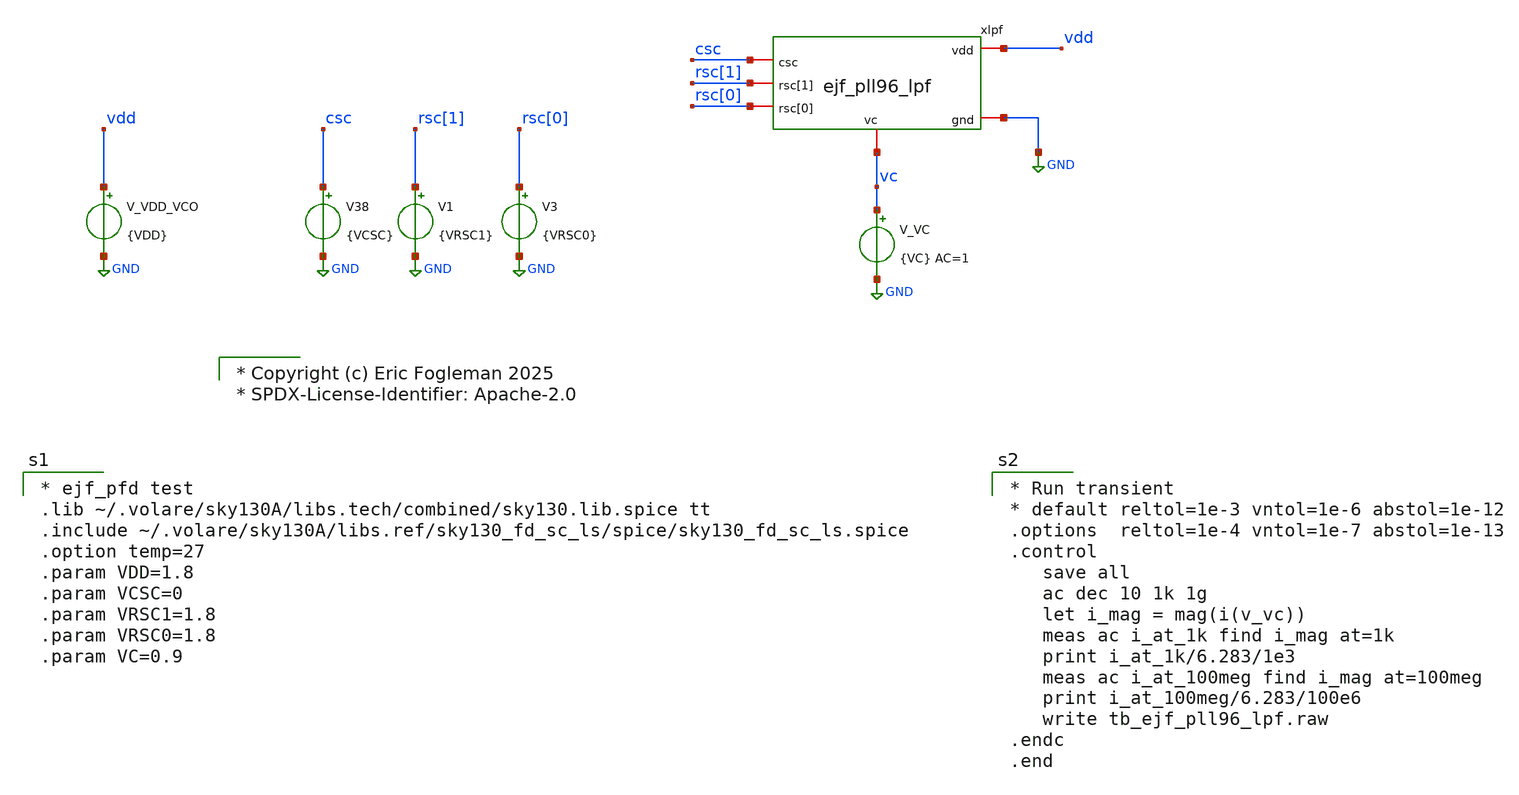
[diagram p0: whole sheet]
** sch_path: xschem/tb_ejf_pll96_lpf.sch
* xschem/ejf_pll96_dbuf.sym:
* Copyright (c) 2025 Eric Fogleman

* Copyright (c) Eric Fogleman 2025
* SPDX-License-Identifier: Apache-2.0

**.subckt tb_ejf_pll96_lpf
V38 csc GND {VCSC}
V_VDD_VCO vdd GND {VDD}
.save i(v_vdd_vco)
xlpf vdd vc GND csc rsc[0] rsc[1] ejf_pll96_lpf
V_VC vc GND {VC} AC=1
.save i(v_vc)
V1 rsc[1] GND {VRSC1}
V3 rsc[0] GND {VRSC0}
**** begin user architecture code

* ejf_pfd test
.lib ~/.volare/sky130A/libs.tech/combined/sky130.lib.spice tt
.include ~/.volare/sky130A/libs.ref/sky130_fd_sc_ls/spice/sky130_fd_sc_ls.spice
.option temp=27
.param VDD=1.8
.param VCSC=0
.param VRSC1=1.8
.param VRSC0=1.8
.param VC=0.9



* Run transient
* default reltol=1e-3 vntol=1e-6 abstol=1e-12
.options  reltol=1e-4 vntol=1e-7 abstol=1e-13
.control
   save all
   ac dec 10 1k 1g
   let i_mag = mag(i(v_vc))
   meas ac i_at_1k find i_mag at=1k
   print i_at_1k/6.283/1e3
   meas ac i_at_100meg find i_mag at=100meg
   print i_at_100meg/6.283/100e6
   write tb_ejf_pll96_lpf.raw
.endc
.end

**** end user architecture code
**.ends

* expanding   symbol:  ejf_pll96_lpf.sym # of pins=6
** sym_path: xschem/ejf_pll96_lpf.sym
** sch_path: xschem/ejf_pll96_lpf.sch
.subckt ejf_pll96_lpf vdd vc gnd csc rsc[0] rsc[1]
*.iopin vc
*.iopin vdd
*.iopin gnd
*.ipin csc
*.ipin rsc[0]
*.ipin rsc[1]
XMPC2[9] vdd mpc2g vdd vdd sky130_fd_pr__pfet_01v8_lvt L=11 W=24 nf=4 ad='int((nf+1)/2) * W/nf * 0.29'
+ as='int((nf+2)/2) * W/nf * 0.29' pd='2*int((nf+1)/2) * (W/nf + 0.29)' ps='2*int((nf+2)/2) * (W/nf + 0.29)'
+ nrd='0.29 / W' nrs='0.29 / W' sa=0 sb=0 sd=0 mult=1 m=1
XMPC2[8] vdd mpc2g vdd vdd sky130_fd_pr__pfet_01v8_lvt L=11 W=24 nf=4 ad='int((nf+1)/2) * W/nf * 0.29'
+ as='int((nf+2)/2) * W/nf * 0.29' pd='2*int((nf+1)/2) * (W/nf + 0.29)' ps='2*int((nf+2)/2) * (W/nf + 0.29)'
+ nrd='0.29 / W' nrs='0.29 / W' sa=0 sb=0 sd=0 mult=1 m=1
XMPC2[7] vdd mpc2g vdd vdd sky130_fd_pr__pfet_01v8_lvt L=11 W=24 nf=4 ad='int((nf+1)/2) * W/nf * 0.29'
+ as='int((nf+2)/2) * W/nf * 0.29' pd='2*int((nf+1)/2) * (W/nf + 0.29)' ps='2*int((nf+2)/2) * (W/nf + 0.29)'
+ nrd='0.29 / W' nrs='0.29 / W' sa=0 sb=0 sd=0 mult=1 m=1
XMPC2[6] vdd mpc2g vdd vdd sky130_fd_pr__pfet_01v8_lvt L=11 W=24 nf=4 ad='int((nf+1)/2) * W/nf * 0.29'
+ as='int((nf+2)/2) * W/nf * 0.29' pd='2*int((nf+1)/2) * (W/nf + 0.29)' ps='2*int((nf+2)/2) * (W/nf + 0.29)'
+ nrd='0.29 / W' nrs='0.29 / W' sa=0 sb=0 sd=0 mult=1 m=1
XMPC2[5] vdd mpc2g vdd vdd sky130_fd_pr__pfet_01v8_lvt L=11 W=24 nf=4 ad='int((nf+1)/2) * W/nf * 0.29'
+ as='int((nf+2)/2) * W/nf * 0.29' pd='2*int((nf+1)/2) * (W/nf + 0.29)' ps='2*int((nf+2)/2) * (W/nf + 0.29)'
+ nrd='0.29 / W' nrs='0.29 / W' sa=0 sb=0 sd=0 mult=1 m=1
XMPC2[4] vdd mpc2g vdd vdd sky130_fd_pr__pfet_01v8_lvt L=11 W=24 nf=4 ad='int((nf+1)/2) * W/nf * 0.29'
+ as='int((nf+2)/2) * W/nf * 0.29' pd='2*int((nf+1)/2) * (W/nf + 0.29)' ps='2*int((nf+2)/2) * (W/nf + 0.29)'
+ nrd='0.29 / W' nrs='0.29 / W' sa=0 sb=0 sd=0 mult=1 m=1
XMPC2[3] vdd mpc2g vdd vdd sky130_fd_pr__pfet_01v8_lvt L=11 W=24 nf=4 ad='int((nf+1)/2) * W/nf * 0.29'
+ as='int((nf+2)/2) * W/nf * 0.29' pd='2*int((nf+1)/2) * (W/nf + 0.29)' ps='2*int((nf+2)/2) * (W/nf + 0.29)'
+ nrd='0.29 / W' nrs='0.29 / W' sa=0 sb=0 sd=0 mult=1 m=1
XMPC2[2] vdd mpc2g vdd vdd sky130_fd_pr__pfet_01v8_lvt L=11 W=24 nf=4 ad='int((nf+1)/2) * W/nf * 0.29'
+ as='int((nf+2)/2) * W/nf * 0.29' pd='2*int((nf+1)/2) * (W/nf + 0.29)' ps='2*int((nf+2)/2) * (W/nf + 0.29)'
+ nrd='0.29 / W' nrs='0.29 / W' sa=0 sb=0 sd=0 mult=1 m=1
XMPC2[1] vdd mpc2g vdd vdd sky130_fd_pr__pfet_01v8_lvt L=11 W=24 nf=4 ad='int((nf+1)/2) * W/nf * 0.29'
+ as='int((nf+2)/2) * W/nf * 0.29' pd='2*int((nf+1)/2) * (W/nf + 0.29)' ps='2*int((nf+2)/2) * (W/nf + 0.29)'
+ nrd='0.29 / W' nrs='0.29 / W' sa=0 sb=0 sd=0 mult=1 m=1
XMPC2[0] vdd mpc2g vdd vdd sky130_fd_pr__pfet_01v8_lvt L=11 W=24 nf=4 ad='int((nf+1)/2) * W/nf * 0.29'
+ as='int((nf+2)/2) * W/nf * 0.29' pd='2*int((nf+1)/2) * (W/nf + 0.29)' ps='2*int((nf+2)/2) * (W/nf + 0.29)'
+ nrd='0.29 / W' nrs='0.29 / W' sa=0 sb=0 sd=0 mult=1 m=1
XMPC1[0] vdd vc vdd vdd sky130_fd_pr__pfet_01v8_lvt L=11 W=24 nf=4 ad='int((nf+1)/2) * W/nf * 0.29' as='int((nf+2)/2) * W/nf * 0.29'
+ pd='2*int((nf+1)/2) * (W/nf + 0.29)' ps='2*int((nf+2)/2) * (W/nf + 0.29)' nrd='0.29 / W' nrs='0.29 / W'
+ sa=0 sb=0 sd=0 mult=1 m=1
XMPC2[18] vdd net5 vdd vdd sky130_fd_pr__pfet_01v8_lvt L=11 W=24 nf=4 ad='int((nf+1)/2) * W/nf * 0.29'
+ as='int((nf+2)/2) * W/nf * 0.29' pd='2*int((nf+1)/2) * (W/nf + 0.29)' ps='2*int((nf+2)/2) * (W/nf + 0.29)'
+ nrd='0.29 / W' nrs='0.29 / W' sa=0 sb=0 sd=0 mult=1 m=1
XMPC2[17] vdd net5 vdd vdd sky130_fd_pr__pfet_01v8_lvt L=11 W=24 nf=4 ad='int((nf+1)/2) * W/nf * 0.29'
+ as='int((nf+2)/2) * W/nf * 0.29' pd='2*int((nf+1)/2) * (W/nf + 0.29)' ps='2*int((nf+2)/2) * (W/nf + 0.29)'
+ nrd='0.29 / W' nrs='0.29 / W' sa=0 sb=0 sd=0 mult=1 m=1
XMPC2[16] vdd net5 vdd vdd sky130_fd_pr__pfet_01v8_lvt L=11 W=24 nf=4 ad='int((nf+1)/2) * W/nf * 0.29'
+ as='int((nf+2)/2) * W/nf * 0.29' pd='2*int((nf+1)/2) * (W/nf + 0.29)' ps='2*int((nf+2)/2) * (W/nf + 0.29)'
+ nrd='0.29 / W' nrs='0.29 / W' sa=0 sb=0 sd=0 mult=1 m=1
XMPC2[15] vdd net5 vdd vdd sky130_fd_pr__pfet_01v8_lvt L=11 W=24 nf=4 ad='int((nf+1)/2) * W/nf * 0.29'
+ as='int((nf+2)/2) * W/nf * 0.29' pd='2*int((nf+1)/2) * (W/nf + 0.29)' ps='2*int((nf+2)/2) * (W/nf + 0.29)'
+ nrd='0.29 / W' nrs='0.29 / W' sa=0 sb=0 sd=0 mult=1 m=1
XMPC2[14] vdd net5 vdd vdd sky130_fd_pr__pfet_01v8_lvt L=11 W=24 nf=4 ad='int((nf+1)/2) * W/nf * 0.29'
+ as='int((nf+2)/2) * W/nf * 0.29' pd='2*int((nf+1)/2) * (W/nf + 0.29)' ps='2*int((nf+2)/2) * (W/nf + 0.29)'
+ nrd='0.29 / W' nrs='0.29 / W' sa=0 sb=0 sd=0 mult=1 m=1
XMPC2[13] vdd net5 vdd vdd sky130_fd_pr__pfet_01v8_lvt L=11 W=24 nf=4 ad='int((nf+1)/2) * W/nf * 0.29'
+ as='int((nf+2)/2) * W/nf * 0.29' pd='2*int((nf+1)/2) * (W/nf + 0.29)' ps='2*int((nf+2)/2) * (W/nf + 0.29)'
+ nrd='0.29 / W' nrs='0.29 / W' sa=0 sb=0 sd=0 mult=1 m=1
XMPC2[12] vdd net5 vdd vdd sky130_fd_pr__pfet_01v8_lvt L=11 W=24 nf=4 ad='int((nf+1)/2) * W/nf * 0.29'
+ as='int((nf+2)/2) * W/nf * 0.29' pd='2*int((nf+1)/2) * (W/nf + 0.29)' ps='2*int((nf+2)/2) * (W/nf + 0.29)'
+ nrd='0.29 / W' nrs='0.29 / W' sa=0 sb=0 sd=0 mult=1 m=1
XMPC2[11] vdd net5 vdd vdd sky130_fd_pr__pfet_01v8_lvt L=11 W=24 nf=4 ad='int((nf+1)/2) * W/nf * 0.29'
+ as='int((nf+2)/2) * W/nf * 0.29' pd='2*int((nf+1)/2) * (W/nf + 0.29)' ps='2*int((nf+2)/2) * (W/nf + 0.29)'
+ nrd='0.29 / W' nrs='0.29 / W' sa=0 sb=0 sd=0 mult=1 m=1
XMPC2[10] vdd net5 vdd vdd sky130_fd_pr__pfet_01v8_lvt L=11 W=24 nf=4 ad='int((nf+1)/2) * W/nf * 0.29'
+ as='int((nf+2)/2) * W/nf * 0.29' pd='2*int((nf+1)/2) * (W/nf + 0.29)' ps='2*int((nf+2)/2) * (W/nf + 0.29)'
+ nrd='0.29 / W' nrs='0.29 / W' sa=0 sb=0 sd=0 mult=1 m=1
XR7[1] vdd vdd vdd sky130_fd_pr__res_high_po_0p35 L=9.9 mult=1 m=1
XR7[0] vdd vdd vdd sky130_fd_pr__res_high_po_0p35 L=9.9 mult=1 m=1
XMPC1[1] vdd net7 vdd vdd sky130_fd_pr__pfet_01v8_lvt L=11 W=24 nf=4 ad='int((nf+1)/2) * W/nf * 0.29'
+ as='int((nf+2)/2) * W/nf * 0.29' pd='2*int((nf+1)/2) * (W/nf + 0.29)' ps='2*int((nf+2)/2) * (W/nf + 0.29)'
+ nrd='0.29 / W' nrs='0.29 / W' sa=0 sb=0 sd=0 mult=1 m=1
x2 vdd csc csc_bb csc_b gnd ejf_pll96_dbuf
XM1 net5 csc_bb mpc2g gnd sky130_fd_pr__nfet_01v8_lvt L=0.15 W=10 nf=1 ad='int((nf+1)/2) * W/nf * 0.29'
+ as='int((nf+2)/2) * W/nf * 0.29' pd='2*int((nf+1)/2) * (W/nf + 0.29)' ps='2*int((nf+2)/2) * (W/nf + 0.29)'
+ nrd='0.29 / W' nrs='0.29 / W' sa=0 sb=0 sd=0 mult=1 m=1
XM2 net7 csc_bb vc gnd sky130_fd_pr__nfet_01v8_lvt L=0.15 W=10 nf=1 ad='int((nf+1)/2) * W/nf * 0.29'
+ as='int((nf+2)/2) * W/nf * 0.29' pd='2*int((nf+1)/2) * (W/nf + 0.29)' ps='2*int((nf+2)/2) * (W/nf + 0.29)'
+ nrd='0.29 / W' nrs='0.29 / W' sa=0 sb=0 sd=0 mult=1 m=1
XR1 vc net4 vdd sky130_fd_pr__res_high_po_0p35 L=9.9 mult=1 m=1
XR2 net4 net2 vdd sky130_fd_pr__res_high_po_0p35 L=9.9 mult=1 m=1
XR3 net2 net1 vdd sky130_fd_pr__res_high_po_0p35 L=9.9 mult=1 m=1
XR4 net1 net3 vdd sky130_fd_pr__res_high_po_0p35 L=9.9 mult=1 m=1
XR5 net3 net6 vdd sky130_fd_pr__res_high_po_0p35 L=9.9 mult=1 m=1
XR6 net6 mpc2g vdd sky130_fd_pr__res_high_po_0p35 L=9.9 mult=1 m=1
XM4 mpc2g rsc_bb[0] net3 gnd sky130_fd_pr__nfet_01v8_lvt L=0.15 W=10 nf=1 ad='int((nf+1)/2) * W/nf * 0.29'
+ as='int((nf+2)/2) * W/nf * 0.29' pd='2*int((nf+1)/2) * (W/nf + 0.29)' ps='2*int((nf+2)/2) * (W/nf + 0.29)'
+ nrd='0.29 / W' nrs='0.29 / W' sa=0 sb=0 sd=0 mult=1 m=1
XM5 mpc2g rsc_bb[1] net1 gnd sky130_fd_pr__nfet_01v8_lvt L=0.15 W=10 nf=1 ad='int((nf+1)/2) * W/nf * 0.29'
+ as='int((nf+2)/2) * W/nf * 0.29' pd='2*int((nf+1)/2) * (W/nf + 0.29)' ps='2*int((nf+2)/2) * (W/nf + 0.29)'
+ nrd='0.29 / W' nrs='0.29 / W' sa=0 sb=0 sd=0 mult=1 m=1
x1[1] vdd rsc[1] rsc_bb[1] rsc_b[1] gnd ejf_pll96_dbuf
x1[0] vdd rsc[0] rsc_bb[0] rsc_b[0] gnd ejf_pll96_dbuf
.ends


* expanding   symbol:  ejf_pll96_dbuf.sym # of pins=5
** sym_path: xschem/ejf_pll96_dbuf.sym
** sch_path: xschem/ejf_pll96_dbuf.sch
.subckt ejf_pll96_dbuf vdd a y y_b gnd
*.ipin a
*.iopin vdd
*.iopin gnd
*.opin y
*.opin y_b
XMP1 y_b a vdd vdd sky130_fd_pr__pfet_01v8_hvt L=0.15 W=2 nf=1 ad='int((nf+1)/2) * W/nf * 0.29' as='int((nf+2)/2) * W/nf * 0.29'
+ pd='2*int((nf+1)/2) * (W/nf + 0.29)' ps='2*int((nf+2)/2) * (W/nf + 0.29)' nrd='0.29 / W' nrs='0.29 / W'
+ sa=0 sb=0 sd=0 mult=1 m=1
XMP3 y y_b vdd vdd sky130_fd_pr__pfet_01v8_hvt L=0.15 W=2 nf=1 ad='int((nf+1)/2) * W/nf * 0.29' as='int((nf+2)/2) * W/nf * 0.29'
+ pd='2*int((nf+1)/2) * (W/nf + 0.29)' ps='2*int((nf+2)/2) * (W/nf + 0.29)' nrd='0.29 / W' nrs='0.29 / W'
+ sa=0 sb=0 sd=0 mult=1 m=1
XMN4 y y_b gnd gnd sky130_fd_pr__nfet_01v8 L=0.15 W=1 nf=1 ad='int((nf+1)/2) * W/nf * 0.29' as='int((nf+2)/2) * W/nf * 0.29'
+ pd='2*int((nf+1)/2) * (W/nf + 0.29)' ps='2*int((nf+2)/2) * (W/nf + 0.29)' nrd='0.29 / W' nrs='0.29 / W'
+ sa=0 sb=0 sd=0 mult=1 m=1
XMN2 y_b a gnd gnd sky130_fd_pr__nfet_01v8 L=0.15 W=1 nf=1 ad='int((nf+1)/2) * W/nf * 0.29' as='int((nf+2)/2) * W/nf * 0.29'
+ pd='2*int((nf+1)/2) * (W/nf + 0.29)' ps='2*int((nf+2)/2) * (W/nf + 0.29)' nrd='0.29 / W' nrs='0.29 / W'
+ sa=0 sb=0 sd=0 mult=1 m=1
**** begin user architecture code

* Copyright (c) Eric Fogleman 2025
* SPDX-License-Identifier: Apache-2.0

**** end user architecture code
.ends

.GLOBAL GND
.end
